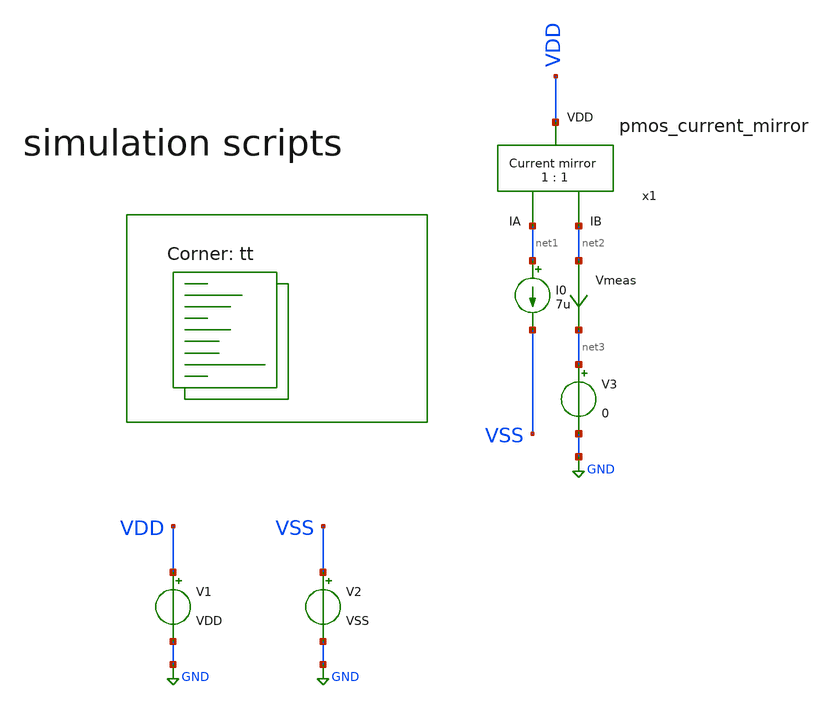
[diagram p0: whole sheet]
** sch_path: Learning/single_ended_amplifiers/Design_transcondutance_cell_sky130_5V/test_layout.sch
**.subckt test_layout
V1 VDD GND VDD
V2 VSS GND VSS
I0 net1 VSS 7u
V3 net3 GND 0
Vmeas net2 net3 0
.save i(vmeas)
x1 VDD net2 net1 pmos_current_mirror
**** begin user architecture code
.lib $::SKYWATER_MODELS/sky130.lib.spice tt


.Temp 27
.param VDD = 5
.param VSS = 0
.include ../../../foss/designs/OSAD/Learning/single_ended_amplifiers/Design_transcondutance_cell_sky130_5V/pmos_current_mirror.spice


.control
save all

save @m.xm2.msky130_fd_pr__nfet_g5v0d10v5[vdsat]

dc V3 0 5 0.001
plot i(Vmeas)





.endc

**** end user architecture code
**.ends
.GLOBAL GND
.end
